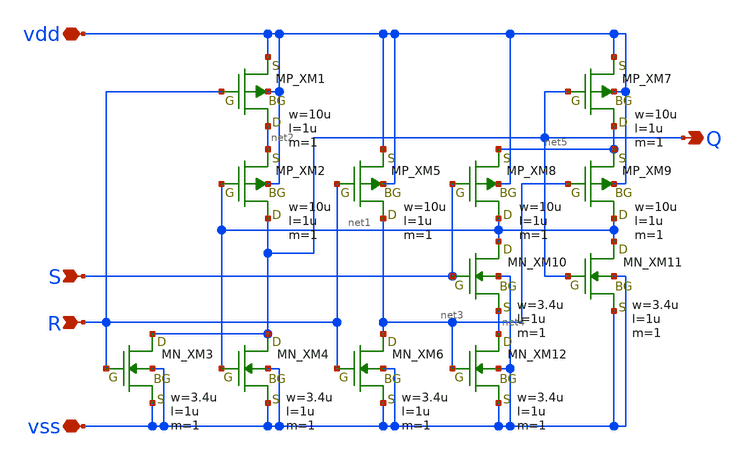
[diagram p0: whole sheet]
** sch_path: member_project/DCDC/ShuntaroOHNO/xschem/prsr_latch.sch
**.subckt prsr_latch vdd vss S R Q
*.iopin vdd
*.iopin vss
*.ipin S
*.ipin R
*.opin Q
XXM1 net2 R vdd vdd PMOS w=10u l=1u as=0 ad=0 ps=0 pd=0 nrd=0 nrs=0 m=1
XXM2 Q net1 net2 vdd PMOS w=10u l=1u as=0 ad=0 ps=0 pd=0 nrd=0 nrs=0 m=1
XXM3 Q R vss vss NMOS w=3.4u l=1u as=0 ad=0 ps=0 pd=0 nrd=0 nrs=0 m=1
XXM4 Q net1 vss vss NMOS w=3.4u l=1u as=0 ad=0 ps=0 pd=0 nrd=0 nrs=0 m=1
XXM5 net3 R vdd vdd PMOS w=10u l=1u as=0 ad=0 ps=0 pd=0 nrd=0 nrs=0 m=1
XXM6 net3 R vss vss NMOS w=3.4u l=1u as=0 ad=0 ps=0 pd=0 nrd=0 nrs=0 m=1
XXM7 net5 Q vdd vdd PMOS w=10u l=1u as=0 ad=0 ps=0 pd=0 nrd=0 nrs=0 m=1
XXM8 net1 S net5 vdd PMOS w=10u l=1u as=0 ad=0 ps=0 pd=0 nrd=0 nrs=0 m=1
XXM9 net1 net3 net5 vdd PMOS w=10u l=1u as=0 ad=0 ps=0 pd=0 nrd=0 nrs=0 m=1
XXM10 net1 S net4 vss NMOS w=3.4u l=1u as=0 ad=0 ps=0 pd=0 nrd=0 nrs=0 m=1
XXM11 net1 Q vss vss NMOS w=3.4u l=1u as=0 ad=0 ps=0 pd=0 nrd=0 nrs=0 m=1
XXM12 net4 net3 vss vss NMOS w=3.4u l=1u as=0 ad=0 ps=0 pd=0 nrd=0 nrs=0 m=1
**.ends
.end
